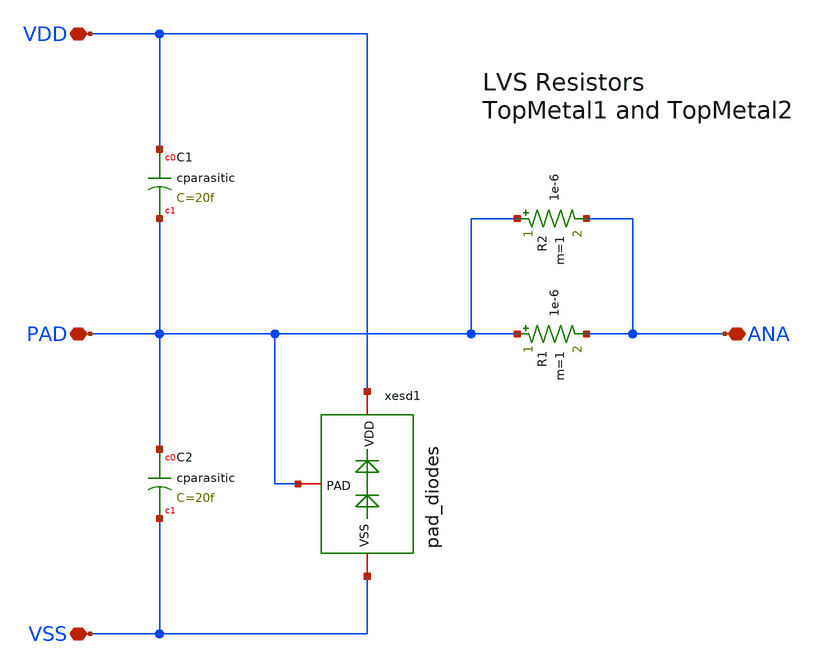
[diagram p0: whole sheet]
** sch_path: JKU_TC1/design_data/xschem/pads/pad_ana.sch
**.subckt pad_ana VSS PAD VDD ANA
*.iopin VSS
*.iopin PAD
*.iopin VDD
*.iopin ANA
XC1 VDD PAD cparasitic C=20f
XC2 PAD VSS cparasitic C=20f
R1 PAD ANA 1e-6 m=1
R2 PAD ANA 1e-6 m=1
xesd1 VDD PAD VSS pad_diodes
**.ends

* expanding   symbol:  pads/pad_diodes.sym # of pins=3
** sym_path: JKU_TC1/design_data/xschem/pads/pad_diodes.sym
** sch_path: JKU_TC1/design_data/xschem/pads/pad_diodes.sch
.subckt pad_diodes VDD PAD VSS
*.iopin VDD
*.iopin VSS
*.iopin PAD
XXD1 PAD VDD dantenna l=780n w=780n
XXD2 VSS PAD dantenna l=780n w=780n
.ends

.end
